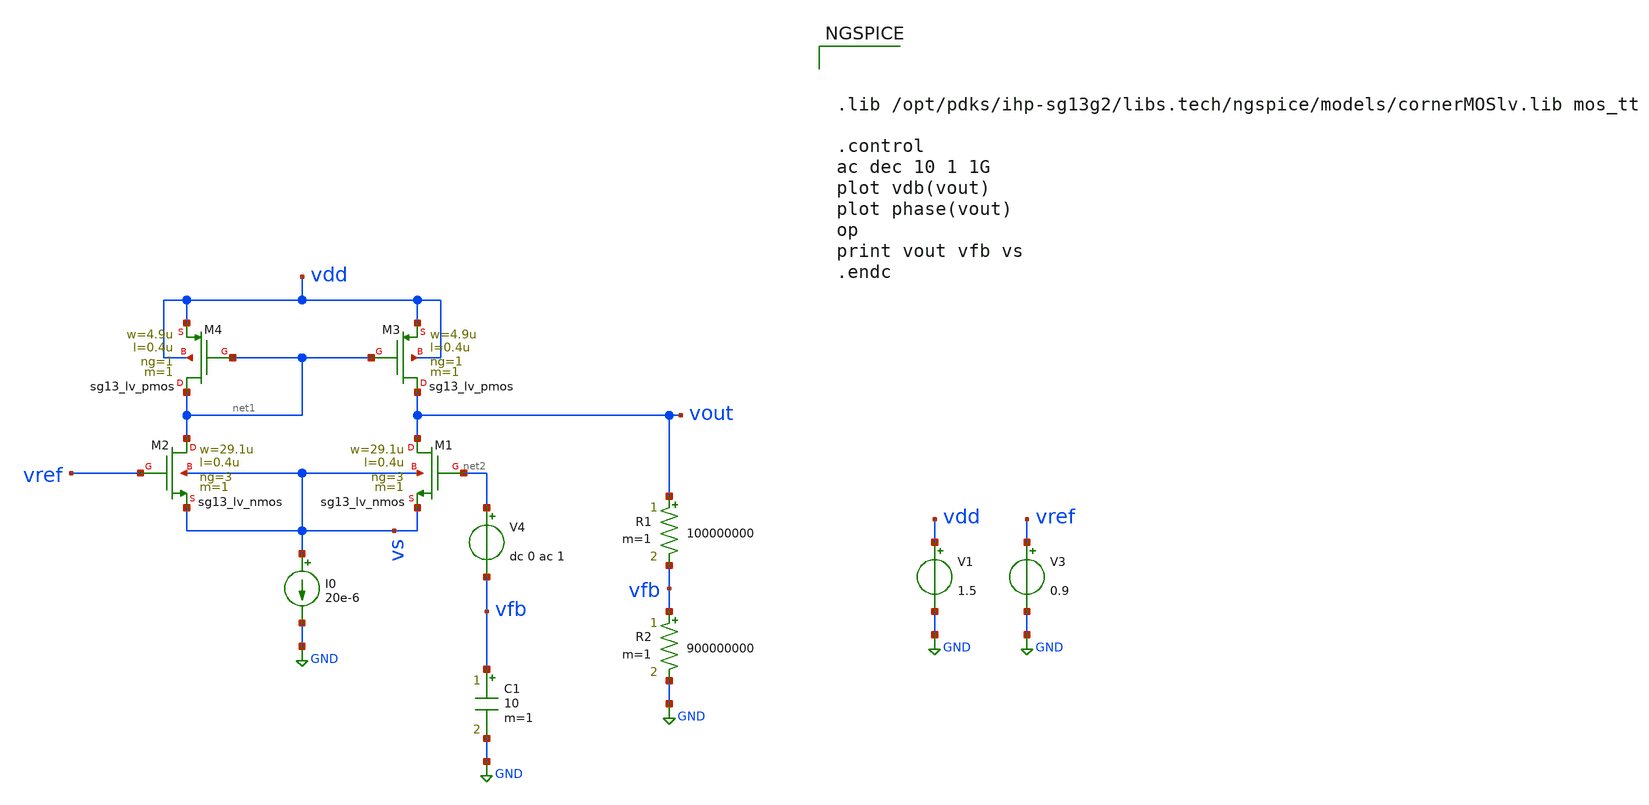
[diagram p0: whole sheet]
** sch_path: test-python/OTA_1stage_opt/xschem/ota_1stage.sch
**.subckt ota_1stage
XM1 vout net2 vs vs sg13_lv_nmos w=29.1u l=0.4u ng=3 m=1 mm_ok=1
XM2 net1 vref vs vs sg13_lv_nmos w=29.1u l=0.4u ng=3 m=1 mm_ok=1
XM3 vout net1 vdd vdd sg13_lv_pmos w=4.9u l=0.4u ng=1 m=1 mm_ok=1
XM4 net1 net1 vdd vdd sg13_lv_pmos w=4.9u l=0.4u ng=1 m=1 mm_ok=1
I0 vs GND 20e-6
V1 vdd GND 1.5
V3 vref GND 0.9
V4 net2 vfb dc 0 ac 1
C1 vfb GND 10 m=1
R1 vout vfb 100000000 m=1
R2 vfb GND 900000000 m=1
**** begin user architecture code



.lib /opt/pdks/ihp-sg13g2/libs.tech/ngspice/models/cornerMOSlv.lib mos_tt

.control
ac dec 10 1 1G
plot vdb(vout)
plot phase(vout)
op
print vout vfb vs
.endc



**** end user architecture code
**.ends
.GLOBAL GND
.end
